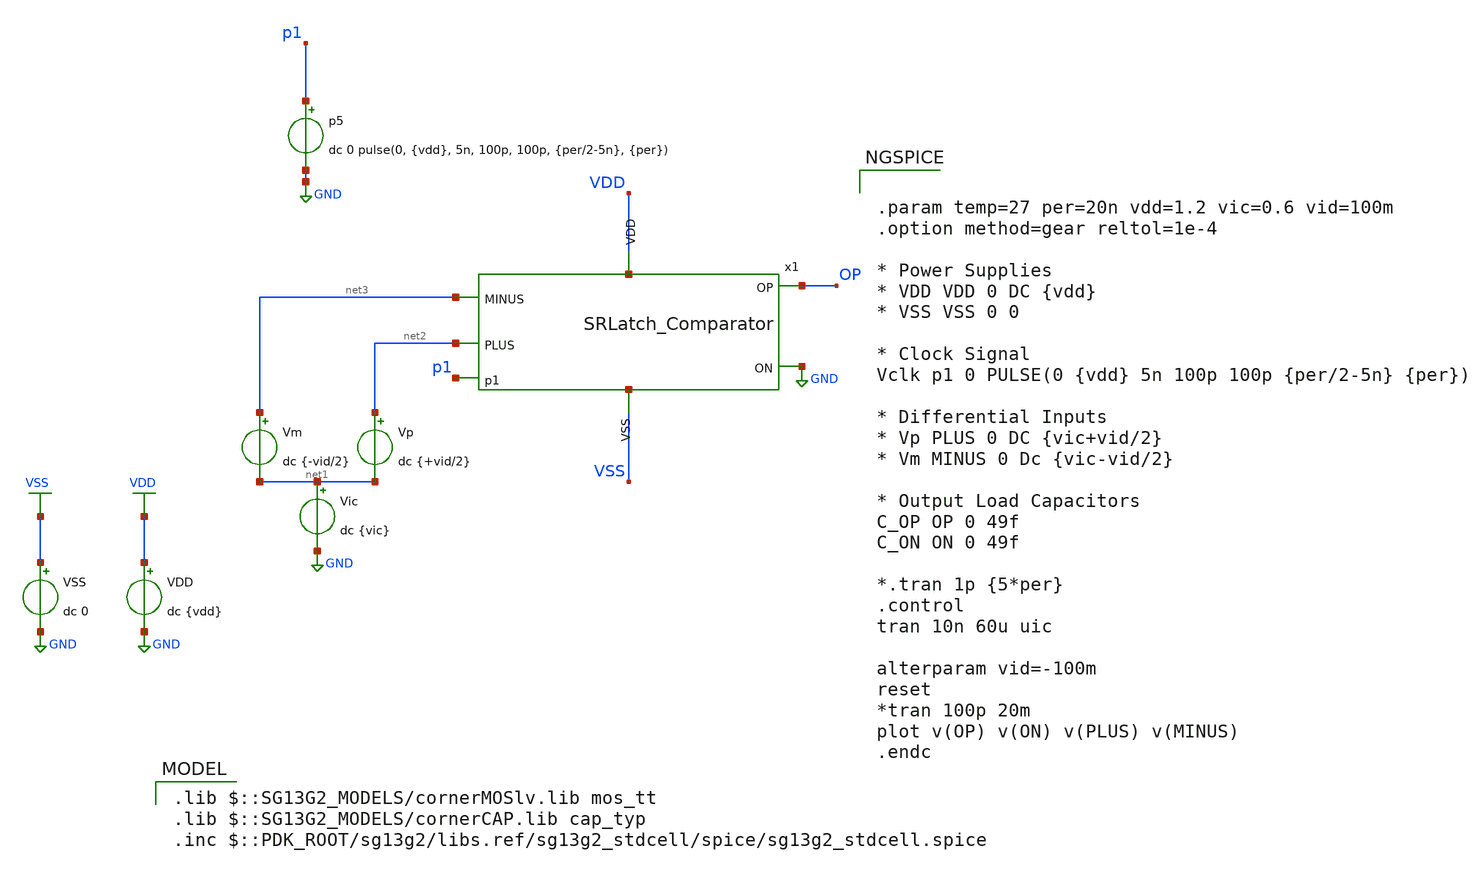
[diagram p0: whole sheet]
** sch_path: DSM/Sneha/tb_SA_Comp.sch
**.subckt tb_SA_Comp
p5 p1 GND dc 0 pulse(0, {vdd}, 5n, 100p, 100p, {per/2-5n}, {per})
VDD VDD GND dc {vdd}
VSS VSS GND dc 0
Vic net1 GND dc {vic}
Vm net3 net1 dc {-vid/2}
Vp net2 net1 dc {+vid/2}
x1 net4 p1 OP GND net3 net2 net5 SRLatch_Comparator
**** begin user architecture code
 .lib $::SG13G2_MODELS/cornerMOSlv.lib mos_tt
.lib $::SG13G2_MODELS/cornerCAP.lib cap_typ
.inc $::PDK_ROOT/sg13g2/libs.ref/sg13g2_stdcell/spice/sg13g2_stdcell.spice



.param temp=27 per=20n vdd=1.2 vic=0.6 vid=100m
.option method=gear reltol=1e-4

* Power Supplies
* VDD VDD 0 DC {vdd}
* VSS VSS 0 0

* Clock Signal
Vclk p1 0 PULSE(0 {vdd} 5n 100p 100p {per/2-5n} {per})

* Differential Inputs
* Vp PLUS 0 DC {vic+vid/2}
* Vm MINUS 0 Dc {vic-vid/2}

* Output Load Capacitors
C_OP OP 0 49f
C_ON ON 0 49f

*.tran 1p {5*per}
.control
tran 10n 60u uic

alterparam vid=-100m
reset
*tran 100p 20m
plot v(OP) v(ON) v(PLUS) v(MINUS)
.endc


**** end user architecture code
**.ends
.GLOBAL GND
.GLOBAL VDD
.GLOBAL VSS
.end
